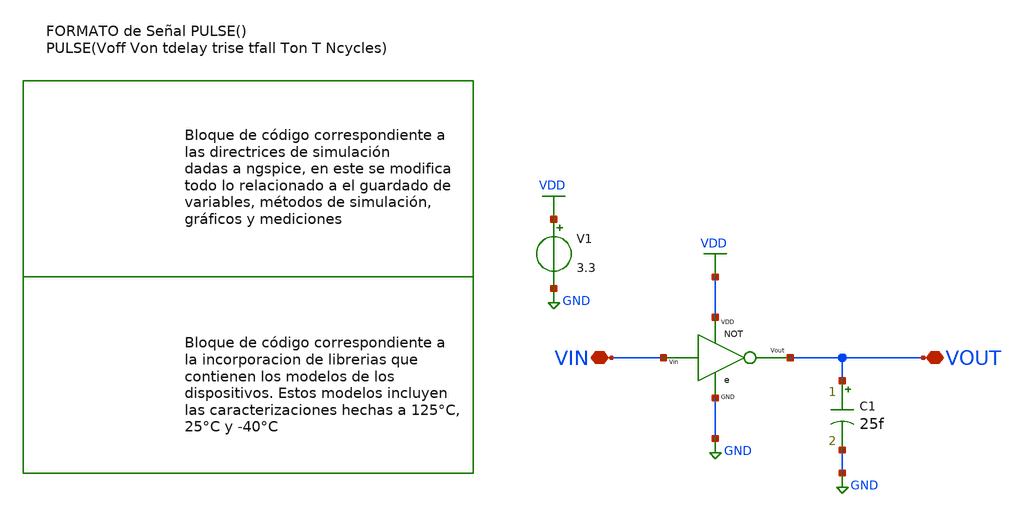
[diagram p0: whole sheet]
** sch_path: xschem/LogicGates/TRAN_NOT.sch
**.subckt TRAN_NOT VOUT VIN
*.iopin VOUT
*.iopin VIN
e VDD VIN VOUT GND NOT
C1 VOUT GND 25f m=1
V1 VDD GND 3.3
**** begin user architecture code


.lib cornerMOShv.lib mos_tt
.lib cornerMOSlv.lib mos_tt
*.lib cornerMOShv.lib mos_ff
*.lib cornerMOSlv.lib mos_ff
*.lib cornerMOShv.lib mos_ss
*.lib cornerMOSlv.lib mos_ss
*.lib cornerMOShv.lib mos_sf
*.lib cornerMOSlv.lib mos_sf
*.lib cornerMOShv.lib mos_fs
*.lib cornerMOSlv.lib mos_fs

*.include /opt/pdks/ihp-sg13g2/libs.ref/sg13g2_stdcell/spice/sg13g2_stdcell.spice
*.lib $::SG13G2_MODELS/cornerRES.lib res_typ
*.lib $::SG13G2_MODELS/cornerCAP.lib cap_typ
*.lib $::SG13G2_MODELS/diodes.lib





vin VIN 0 PULSE(0 3.3 1ns 0ns 0ns 2ns 4ns)

.control

save all
***********************************************
* SIMULACION DE 10 NANO DE DURACION, CON MEDICIONES CADA 100 PICO
tran 100ps 10ns

**********************************************

plot V(VIN) v(VOUT)

**********************************************
*COMANDOS PARA MEDIR EL TIEMPO DE PROPAGACIÓN DE LA COMPUERTA

meas tran tpLH_in FIND time WHEN v(VIN)=1.65 TD=0 FALL=1
meas tran tpLH_fin FIND time WHEN v(VOUT)=1.65 TD=0 RISE=1
meas tran tpHL_in FIND time WHEN v(VIN)=1.65 TD=0 RISE=1
meas tran tpHL_fin FIND time WHEN v(VOUT)=1.65 TD=0 FALL=1
print tpHL_fin - tpHL_in
print tpLH_fin - tpLH_in
**********************************************
.endc


**** end user architecture code
**.ends

* expanding   symbol:  ../LogicGates/NOT.sym # of pins=4
** sym_path: xschem/LogicGates/NOT.sym
** sch_path: xschem/LogicGates/NOT.sch
.subckt NOT VDD Vin Vout GND
*.ipin VDD
*.ipin Vin
*.ipin GND
*.opin Vout
XM3 GND Vin Vout GND sg13_hv_nmos w=10.0u l=5u ng=1 m=1 mm_ok=1
XM4 Vout Vin VDD VDD sg13_hv_pmos w=2.72u l=0.45u ng=1 m=1 mm_ok=1
.ends

.GLOBAL VDD
.GLOBAL GND
.end
